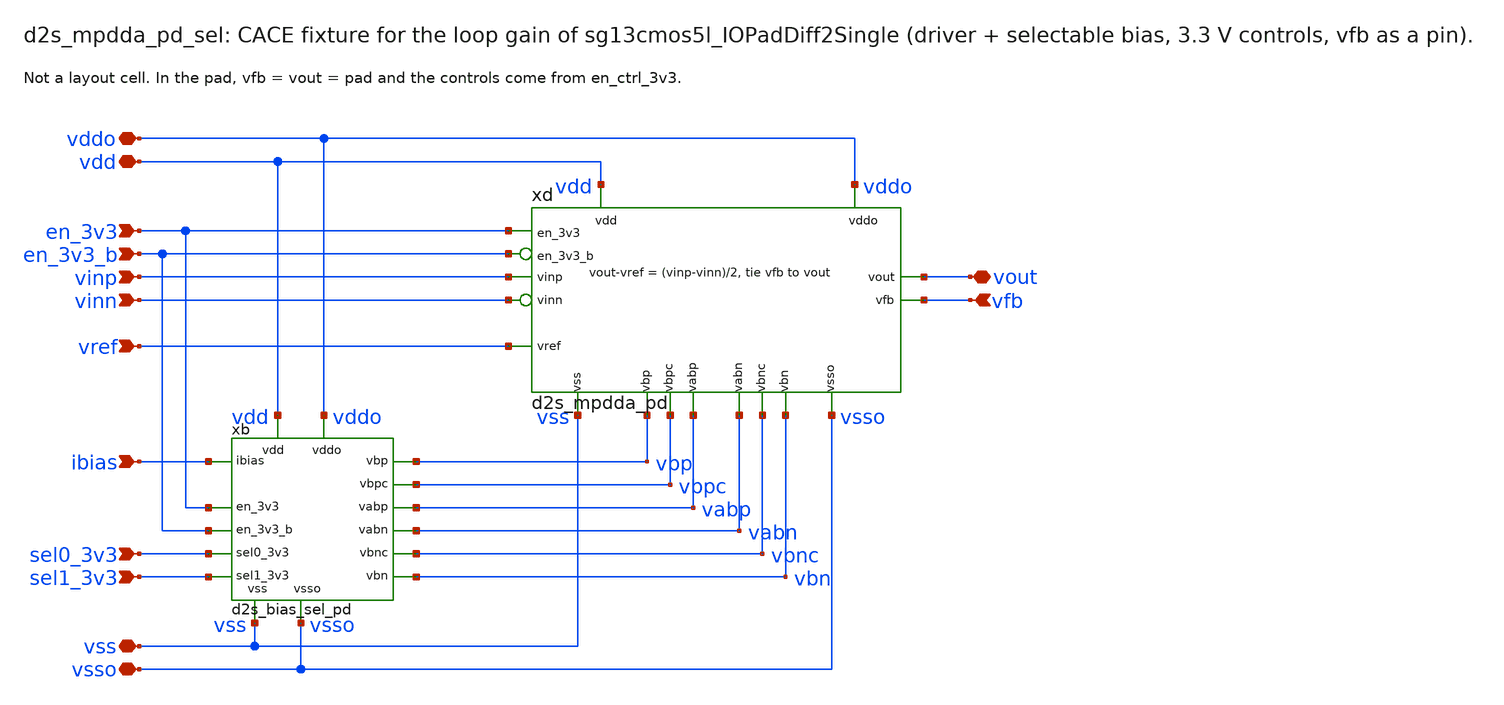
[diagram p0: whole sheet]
** sch_path: sudelbuecher/design_considerations/consolidation/bias_hierarchy_2026-10-27/before/macros/sg13cmos5l_IOPadDiff2Single/schematic/xschem/d2s_mpdda_pd_sel.sch
**.subckt d2s_mpdda_pd_sel vdd vss vddo vsso vinp vinn vref vout vfb ibias en_3v3 sel0_3v3 sel1_3v3
*+ en_3v3_b
*.iopin vdd
*.iopin vss
*.iopin vddo
*.iopin vsso
*.ipin vinp
*.ipin vinn
*.ipin vref
*.iopin vout
*.ipin vfb
*.ipin ibias
*.ipin en_3v3
*.ipin sel0_3v3
*.ipin sel1_3v3
*.ipin en_3v3_b
xb vdd vss vddo vsso ibias vbp vbn vbpc vbnc vabp vabn en_3v3 sel0_3v3 sel1_3v3 en_3v3_b
+ d2s_bias_sel_pd
xd vdd vss vddo vsso vinp vinn vref vout vfb vbp vbn vbpc vbnc vabp vabn en_3v3 en_3v3_b
+ d2s_mpdda_pd
**.ends
.end
